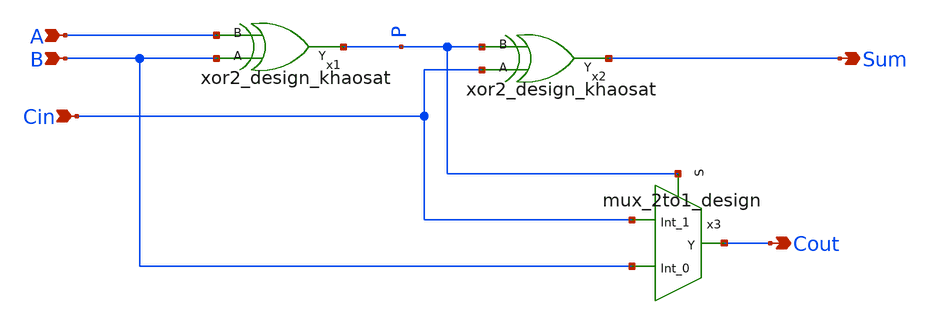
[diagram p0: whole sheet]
** sch_path: cells/full_adder_tg/xschem/Full_adder_1bit.sch
**.subckt Full_adder_1bit B A Cin Sum Cout
*.ipin B
*.ipin A
*.ipin Cin
*.opin Sum
*.opin Cout
x1 A B P xor2_design_khaosat
x2 P Cin Sum xor2_design_khaosat
x3 Cin Cout P B mux_2to1_design
**.ends

* expanding   symbol:  ./xor2_design_khaosat.sym # of pins=3
** sym_path: cells/full_adder_tg/xschem/xor2_design_khaosat.sym
** sch_path: cells/full_adder_tg/xschem/xor2_design_khaosat.sch
.subckt xor2_design_khaosat B A Y
*.opin Y
*.ipin B
*.ipin A
XMPmos_inv_1 net1 B VDD VDD sky130_fd_pr__pfet_01v8 L=0.15 W=5 nf=1 ad='int((1 + 1)/2) * 5 / 1 * 0.29'
+ as='int((1 + 2)/2) * 5 / 1 * 0.29' pd='2*int((1 + 1)/2) * (5 / 1 + 0.29)' ps='2*int((1 + 2)/2) * (5 / 1 + 0.29)'
+ nrd='0.29 / 5 ' nrs='0.29 / 5 ' sa=0 sb=0 sd=0 mult=1 m=1
XMNmos_inv_1 net1 B 0 0 sky130_fd_pr__nfet_01v8 L=0.15 W=2 nf=1 ad='int((1 + 1)/2) * 2 / 1 * 0.29' as='int((1 + 2)/2) * 2 / 1 * 0.29'
+ pd='2*int((1 + 1)/2) * (2 / 1 + 0.29)' ps='2*int((1 + 2)/2) * (2 / 1 + 0.29)' nrd='0.29 / 2 ' nrs='0.29 / 2 '
+ sa=0 sb=0 sd=0 mult=1 m=1
XMPmos_xor_1 Y B A VDD sky130_fd_pr__pfet_01v8 L=0.15 W=5 nf=1 ad='int((1 + 1)/2) * 5 / 1 * 0.29' as='int((1 + 2)/2) * 5 / 1 * 0.29'
+ pd='2*int((1 + 1)/2) * (5 / 1 + 0.29)' ps='2*int((1 + 2)/2) * (5 / 1 + 0.29)' nrd='0.29 / 5 ' nrs='0.29 / 5 '
+ sa=0 sb=0 sd=0 mult=1 m=1
XMNmos_xor_1 Y net1 A 0 sky130_fd_pr__nfet_01v8 L=0.15 W=2 nf=1 ad='int((1 + 1)/2) * 2 / 1 * 0.29' as='int((1 + 2)/2) * 2 / 1 * 0.29'
+ pd='2*int((1 + 1)/2) * (2 / 1 + 0.29)' ps='2*int((1 + 2)/2) * (2 / 1 + 0.29)' nrd='0.29 / 2 ' nrs='0.29 / 2 '
+ sa=0 sb=0 sd=0 mult=1 m=1
XMPmos_xor_2 Y A B VDD sky130_fd_pr__pfet_01v8 L=0.15 W=5 nf=1 ad='int((1 + 1)/2) * 5 / 1 * 0.29' as='int((1 + 2)/2) * 5 / 1 * 0.29'
+ pd='2*int((1 + 1)/2) * (5 / 1 + 0.29)' ps='2*int((1 + 2)/2) * (5 / 1 + 0.29)' nrd='0.29 / 5 ' nrs='0.29 / 5 '
+ sa=0 sb=0 sd=0 mult=1 m=1
XMNmos_xor_2 Y A net1 0 sky130_fd_pr__nfet_01v8 L=0.15 W=2 nf=1 ad='int((1 + 1)/2) * 2 / 1 * 0.29' as='int((1 + 2)/2) * 2 / 1 * 0.29'
+ pd='2*int((1 + 1)/2) * (2 / 1 + 0.29)' ps='2*int((1 + 2)/2) * (2 / 1 + 0.29)' nrd='0.29 / 2 ' nrs='0.29 / 2 '
+ sa=0 sb=0 sd=0 mult=1 m=1
.ends


* expanding   symbol:  ./mux_2to1_design.sym # of pins=4
** sym_path: cells/full_adder_tg/xschem/mux_2to1_design.sym
** sch_path: cells/full_adder_tg/xschem/mux_2to1_design.sch
.subckt mux_2to1_design Int_1 Y S Int_0
*.ipin Int_1
*.ipin Int_0
*.opin Y
*.ipin S
XMNmos_1 Y S Int_1 0 sky130_fd_pr__nfet_01v8 L=0.15 W=2 nf=1 ad='int((1 + 1)/2) * 2 / 1 * 0.29' as='int((1 + 2)/2) * 2 / 1 * 0.29'
+ pd='2*int((1 + 1)/2) * (2 / 1 + 0.29)' ps='2*int((1 + 2)/2) * (2 / 1 + 0.29)' nrd='0.29 / 2 ' nrs='0.29 / 2 '
+ sa=0 sb=0 sd=0 mult=1 m=1
XMPmos_1 Y net1 Int_1 VDD sky130_fd_pr__pfet_01v8 L=0.15 W=5 nf=1 ad='int((1 + 1)/2) * 5 / 1 * 0.29'
+ as='int((1 + 2)/2) * 5 / 1 * 0.29' pd='2*int((1 + 1)/2) * (5 / 1 + 0.29)' ps='2*int((1 + 2)/2) * (5 / 1 + 0.29)'
+ nrd='0.29 / 5 ' nrs='0.29 / 5 ' sa=0 sb=0 sd=0 mult=1 m=1
XMNmos_2 Y net1 Int_0 0 sky130_fd_pr__nfet_01v8 L=0.15 W=2 nf=1 ad='int((1 + 1)/2) * 2 / 1 * 0.29' as='int((1 + 2)/2) * 2 / 1 * 0.29'
+ pd='2*int((1 + 1)/2) * (2 / 1 + 0.29)' ps='2*int((1 + 2)/2) * (2 / 1 + 0.29)' nrd='0.29 / 2 ' nrs='0.29 / 2 '
+ sa=0 sb=0 sd=0 mult=1 m=1
XMPmos_2 Y S Int_0 VDD sky130_fd_pr__pfet_01v8 L=0.15 W=5 nf=1 ad='int((1 + 1)/2) * 5 / 1 * 0.29' as='int((1 + 2)/2) * 5 / 1 * 0.29'
+ pd='2*int((1 + 1)/2) * (5 / 1 + 0.29)' ps='2*int((1 + 2)/2) * (5 / 1 + 0.29)' nrd='0.29 / 5 ' nrs='0.29 / 5 '
+ sa=0 sb=0 sd=0 mult=1 m=1
x1 net1 S inveter_design
.ends


* expanding   symbol:  ./inveter_design.sym # of pins=2
** sym_path: cells/full_adder_tg/xschem/inveter_design.sym
** sch_path: cells/full_adder_tg/xschem/inveter_design.sch
.subckt inveter_design Out In
*.ipin In
*.opin Out
XMNMOS Out In 0 0 sky130_fd_pr__nfet_01v8 L=0.15 W=2 nf=1 ad='int((1 + 1)/2) * 2 / 1 * 0.29' as='int((1 + 2)/2) * 2 / 1 * 0.29'
+ pd='2*int((1 + 1)/2) * (2 / 1 + 0.29)' ps='2*int((1 + 2)/2) * (2 / 1 + 0.29)' nrd='0.29 / 2 ' nrs='0.29 / 2 '
+ sa=0 sb=0 sd=0 mult=1 m=1
XMPMOS Out In VDD VDD sky130_fd_pr__pfet_01v8 L=0.15 W=5 nf=1 ad='int((1 + 1)/2) * 5 / 1 * 0.29' as='int((1 + 2)/2) * 5 / 1 * 0.29'
+ pd='2*int((1 + 1)/2) * (5 / 1 + 0.29)' ps='2*int((1 + 2)/2) * (5 / 1 + 0.29)' nrd='0.29 / 5 ' nrs='0.29 / 5 '
+ sa=0 sb=0 sd=0 mult=1 m=1
.ends

.GLOBAL VDD
.end
